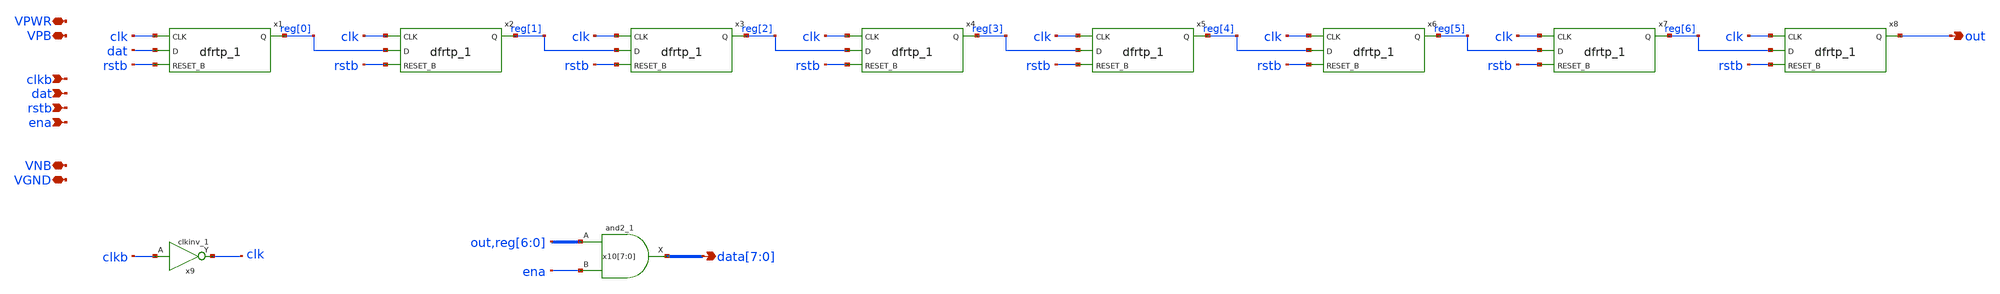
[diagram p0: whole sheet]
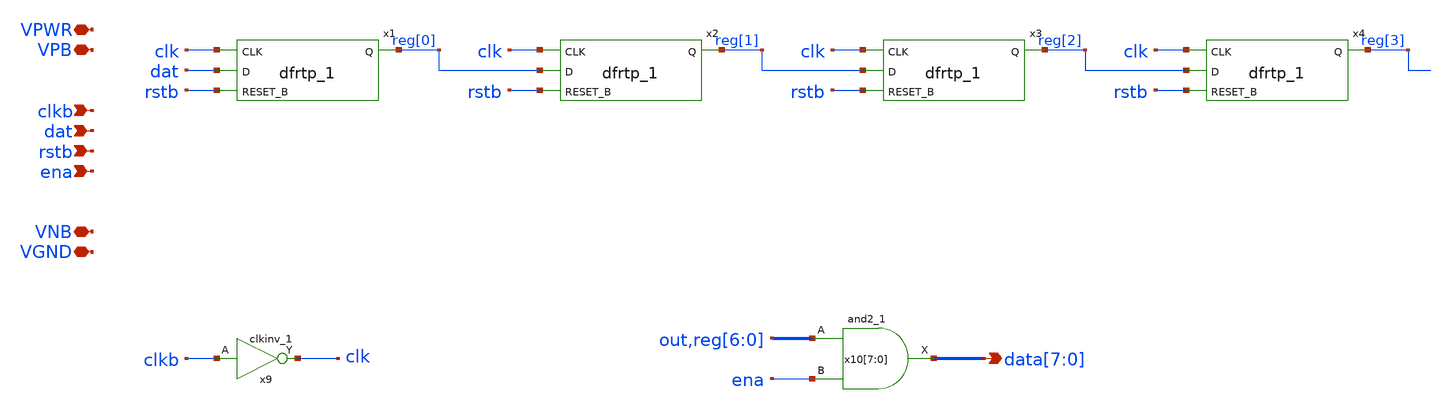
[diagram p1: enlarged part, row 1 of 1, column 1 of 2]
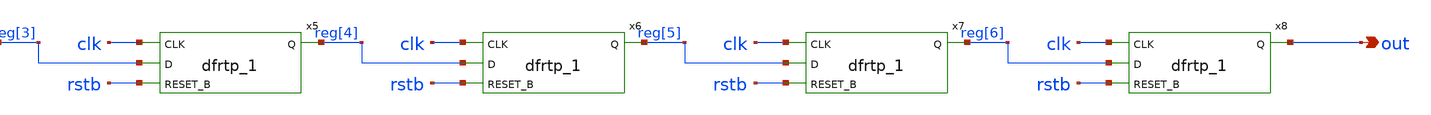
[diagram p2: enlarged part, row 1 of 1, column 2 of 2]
** sch_path: tt_um_mosbius/xschem/shift_reg_len8.sch
**.subckt shift_reg_len8 clkb dat rstb VPWR
*+ data[7],data[6],data[5],data[4],data[3],data[2],data[1],data[0] ena out VGND VPB VNB
*.ipin clkb
*.ipin dat
*.ipin rstb
*.iopin VPWR
*.opin data[7],data[6],data[5],data[4],data[3],data[2],data[1],data[0]
*.ipin ena
*.opin out
*.iopin VGND
*.iopin VPB
*.iopin VNB
x10[7] out ena VGND VNB VPB VPWR data[7] sky130_fd_sc_hd__and2_1
x10[6] reg[6] ena VGND VNB VPB VPWR data[6] sky130_fd_sc_hd__and2_1
x10[5] reg[5] ena VGND VNB VPB VPWR data[5] sky130_fd_sc_hd__and2_1
x10[4] reg[4] ena VGND VNB VPB VPWR data[4] sky130_fd_sc_hd__and2_1
x10[3] reg[3] ena VGND VNB VPB VPWR data[3] sky130_fd_sc_hd__and2_1
x10[2] reg[2] ena VGND VNB VPB VPWR data[2] sky130_fd_sc_hd__and2_1
x10[1] reg[1] ena VGND VNB VPB VPWR data[1] sky130_fd_sc_hd__and2_1
x10[0] reg[0] ena VGND VNB VPB VPWR data[0] sky130_fd_sc_hd__and2_1
x1 clk dat rstb VGND VNB VPB VPWR reg[0] sky130_fd_sc_hd__dfrtp_1
x2 clk reg[0] rstb VGND VNB VPB VPWR reg[1] sky130_fd_sc_hd__dfrtp_1
x3 clk reg[1] rstb VGND VNB VPB VPWR reg[2] sky130_fd_sc_hd__dfrtp_1
x4 clk reg[2] rstb VGND VNB VPB VPWR reg[3] sky130_fd_sc_hd__dfrtp_1
x5 clk reg[3] rstb VGND VNB VPB VPWR reg[4] sky130_fd_sc_hd__dfrtp_1
x6 clk reg[4] rstb VGND VNB VPB VPWR reg[5] sky130_fd_sc_hd__dfrtp_1
x7 clk reg[5] rstb VGND VNB VPB VPWR reg[6] sky130_fd_sc_hd__dfrtp_1
x8 clk reg[6] rstb VGND VNB VPB VPWR out sky130_fd_sc_hd__dfrtp_1
x9 clkb VGND VNB VPB VPWR clk sky130_fd_sc_hd__clkinv_1
**.ends
.end
